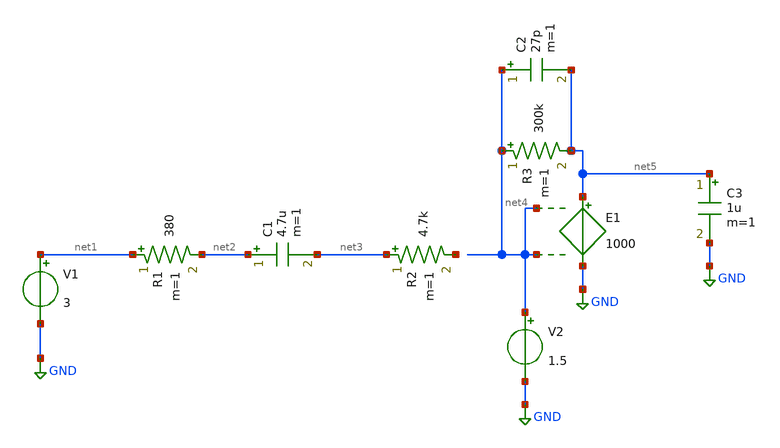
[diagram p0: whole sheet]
** sch_path: xschem/untitled.sch
**.subckt untitled
R1 net1 net2 380 m=1
V1 net1 GND 3
R2 net3 net6 4.7k m=1
C1 net2 net3 4.7u m=1
E1 net5 GND net4 net4 1000
R3 net4 net5 300k m=1
C2 net4 net5 27p m=1
V2 net4 GND 1.5
C3 net5 GND 1u m=1
**.ends
.GLOBAL GND
.end
